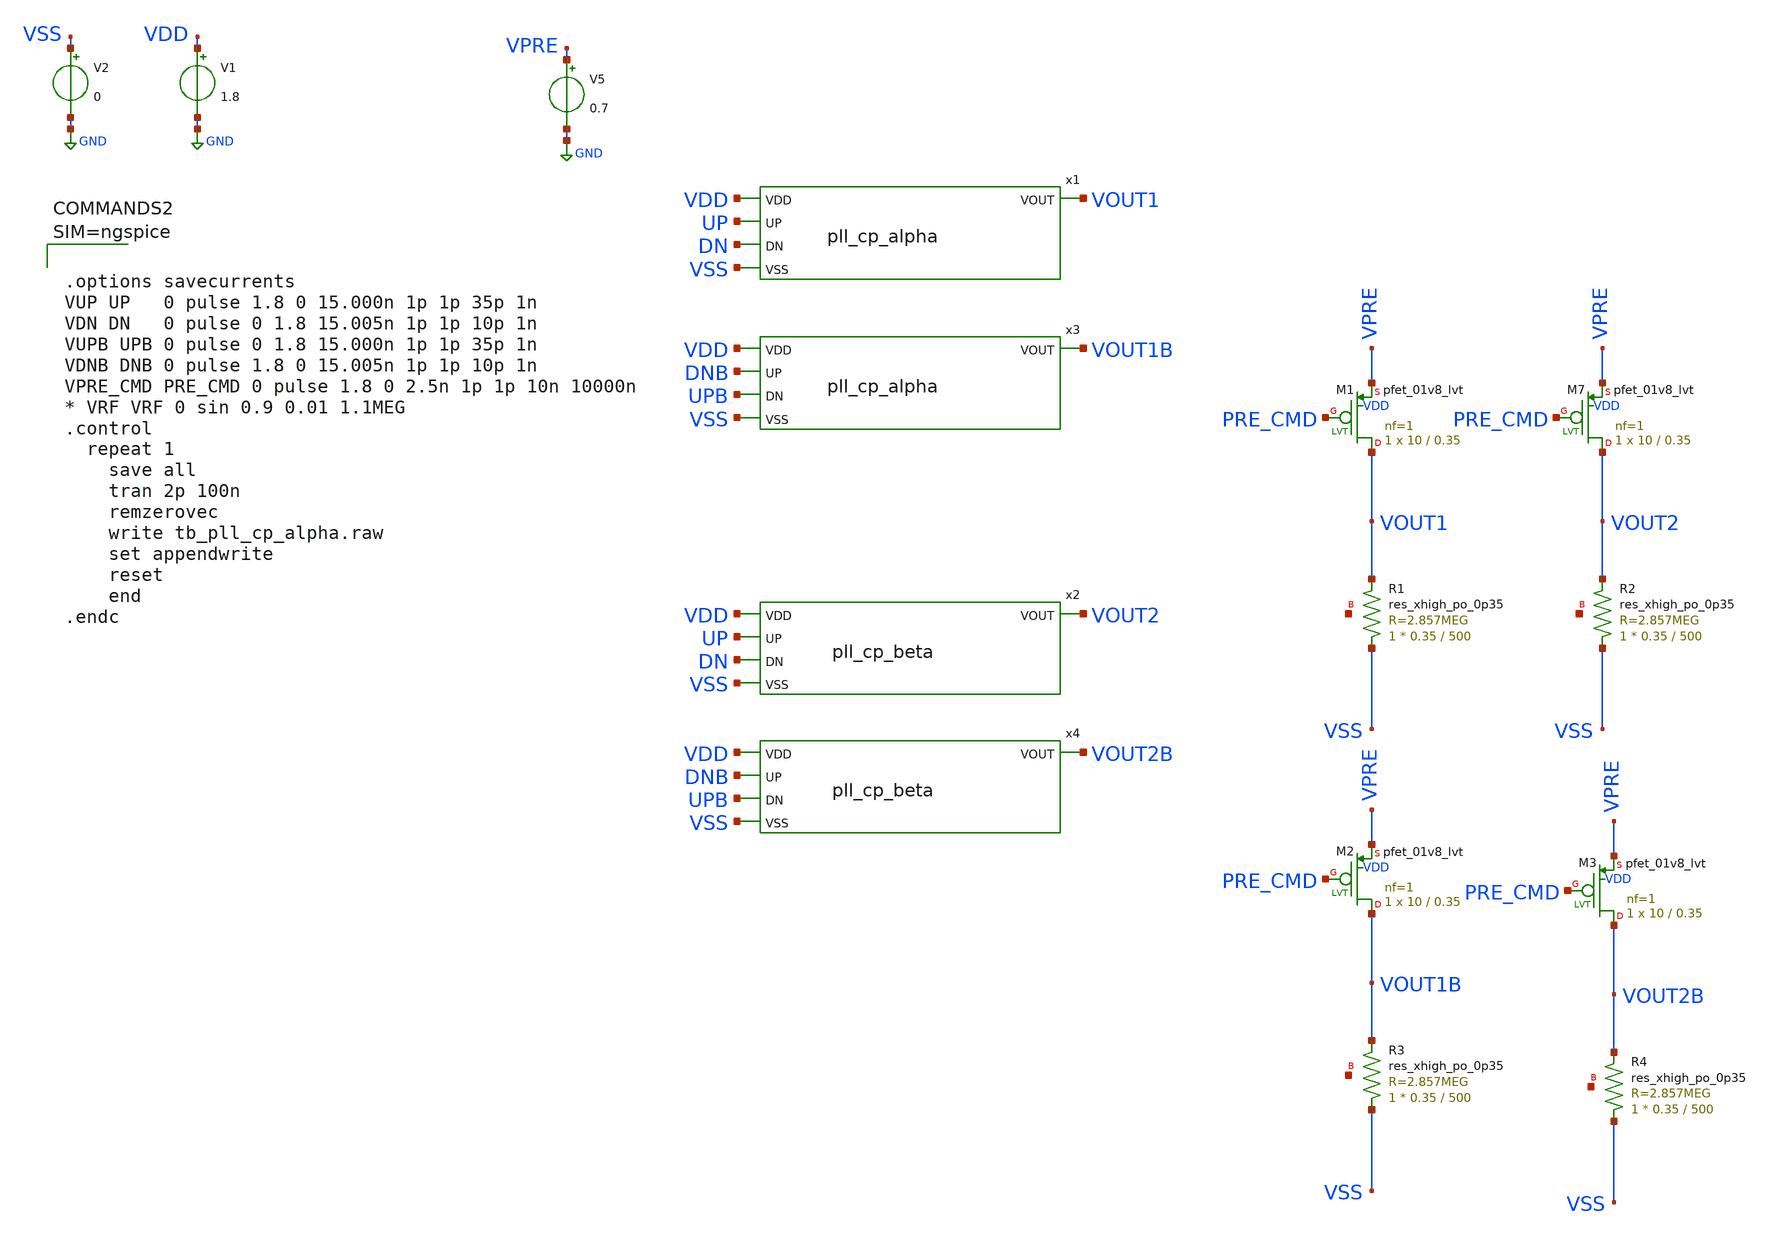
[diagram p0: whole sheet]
** sch_path: xschem/tb_pll_cp_alpha.sch
**.subckt tb_pll_cp_alpha
V1 VDD GND 1.8
V2 VSS GND 0
XR2 VSS VOUT2 net1 sky130_fd_pr__res_xhigh_po_0p35 L=500 mult=1 m=1
XM7 VOUT2 PRE_CMD VPRE VDD sky130_fd_pr__pfet_01v8_lvt L=0.35 W=10 nf=1 ad='int((nf+1)/2) * W/nf * 0.29'
+ as='int((nf+2)/2) * W/nf * 0.29' pd='2*int((nf+1)/2) * (W/nf + 0.29)' ps='2*int((nf+2)/2) * (W/nf + 0.29)'
+ nrd='0.29 / W' nrs='0.29 / W' sa=0 sb=0 sd=0 mult=1 m=1
V5 VPRE GND 0.7
x1 VDD UP DN VOUT1 VSS pll_cp_alpha
x2 VDD UP DN VOUT2 VSS pll_cp_beta
XR1 VSS VOUT1 net2 sky130_fd_pr__res_xhigh_po_0p35 L=500 mult=1 m=1
XM1 VOUT1 PRE_CMD VPRE VDD sky130_fd_pr__pfet_01v8_lvt L=0.35 W=10 nf=1 ad='int((nf+1)/2) * W/nf * 0.29'
+ as='int((nf+2)/2) * W/nf * 0.29' pd='2*int((nf+1)/2) * (W/nf + 0.29)' ps='2*int((nf+2)/2) * (W/nf + 0.29)'
+ nrd='0.29 / W' nrs='0.29 / W' sa=0 sb=0 sd=0 mult=1 m=1
x3 VDD DNB UPB VOUT1B VSS pll_cp_alpha
XR3 VSS VOUT1B net3 sky130_fd_pr__res_xhigh_po_0p35 L=500 mult=1 m=1
XM2 VOUT1B PRE_CMD VPRE VDD sky130_fd_pr__pfet_01v8_lvt L=0.35 W=10 nf=1 ad='int((nf+1)/2) * W/nf * 0.29'
+ as='int((nf+2)/2) * W/nf * 0.29' pd='2*int((nf+1)/2) * (W/nf + 0.29)' ps='2*int((nf+2)/2) * (W/nf + 0.29)'
+ nrd='0.29 / W' nrs='0.29 / W' sa=0 sb=0 sd=0 mult=1 m=1
x4 VDD DNB UPB VOUT2B VSS pll_cp_beta
XR4 VSS VOUT2B net4 sky130_fd_pr__res_xhigh_po_0p35 L=500 mult=1 m=1
XM3 VOUT2B PRE_CMD VPRE VDD sky130_fd_pr__pfet_01v8_lvt L=0.35 W=10 nf=1 ad='int((nf+1)/2) * W/nf * 0.29'
+ as='int((nf+2)/2) * W/nf * 0.29' pd='2*int((nf+1)/2) * (W/nf + 0.29)' ps='2*int((nf+2)/2) * (W/nf + 0.29)'
+ nrd='0.29 / W' nrs='0.29 / W' sa=0 sb=0 sd=0 mult=1 m=1
**** begin user architecture code

** opencircuitdesign pdks install
.lib $::SKYWATER_MODELS/sky130.lib.spice tt_mm





.options savecurrents
VUP UP   0 pulse 1.8 0 15.000n 1p 1p 35p 1n
VDN DN   0 pulse 0 1.8 15.005n 1p 1p 10p 1n
VUPB UPB 0 pulse 0 1.8 15.000n 1p 1p 35p 1n
VDNB DNB 0 pulse 1.8 0 15.005n 1p 1p 10p 1n
VPRE_CMD PRE_CMD 0 pulse 1.8 0 2.5n 1p 1p 10n 10000n
* VRF VRF 0 sin 0.9 0.01 1.1MEG
.control
  repeat 1
    save all
    tran 2p 100n
    remzerovec
    write tb_pll_cp_alpha.raw
    set appendwrite
    reset
    end
.endc



**** end user architecture code
**.ends

* expanding   symbol:  pll_cp_alpha.sym # of pins=5
** sym_path: xschem/pll_cp_alpha.sym
** sch_path: xschem/pll_cp_alpha.sch
.subckt pll_cp_alpha VDD UP DN VOUT VSS
*.ipin UP
*.opin VOUT
*.ipin DN
*.ipin VDD
*.ipin VSS
XM5 VDD DN VLOW VSS sky130_fd_pr__nfet_01v8_lvt L=0.35 W=5 nf=1 ad='int((nf+1)/2) * W/nf * 0.29' as='int((nf+2)/2) * W/nf * 0.29'
+ pd='2*int((nf+1)/2) * (W/nf + 0.29)' ps='2*int((nf+2)/2) * (W/nf + 0.29)' nrd='0.29 / W' nrs='0.29 / W'
+ sa=0 sb=0 sd=0 mult=1 m=1
XM6 net2 VBL net5 VSS sky130_fd_pr__nfet_01v8_lvt L=0.35 W=5 nf=1 ad='int((nf+1)/2) * W/nf * 0.29' as='int((nf+2)/2) * W/nf * 0.29'
+ pd='2*int((nf+1)/2) * (W/nf + 0.29)' ps='2*int((nf+2)/2) * (W/nf + 0.29)' nrd='0.29 / W' nrs='0.29 / W'
+ sa=0 sb=0 sd=0 mult=1 m=1
XM10 net1 net3 VSS VSS sky130_fd_pr__nfet_01v8_lvt L=1 W=2 nf=1 ad='int((nf+1)/2) * W/nf * 0.29' as='int((nf+2)/2) * W/nf * 0.29'
+ pd='2*int((nf+1)/2) * (W/nf + 0.29)' ps='2*int((nf+2)/2) * (W/nf + 0.29)' nrd='0.29 / W' nrs='0.29 / W'
+ sa=0 sb=0 sd=0 mult=1 m=1
vbias1 VLOW net1 0
.save i(vbias1)
XM1 net2 VBH net6 VDD sky130_fd_pr__pfet_01v8_lvt L=0.35 W=10 nf=1 ad='int((nf+1)/2) * W/nf * 0.29' as='int((nf+2)/2) * W/nf * 0.29'
+ pd='2*int((nf+1)/2) * (W/nf + 0.29)' ps='2*int((nf+2)/2) * (W/nf + 0.29)' nrd='0.29 / W' nrs='0.29 / W'
+ sa=0 sb=0 sd=0 mult=1 m=1
XM2 VSS UP VHIGH VDD sky130_fd_pr__pfet_01v8_lvt L=0.35 W=10 nf=1 ad='int((nf+1)/2) * W/nf * 0.29' as='int((nf+2)/2) * W/nf * 0.29'
+ pd='2*int((nf+1)/2) * (W/nf + 0.29)' ps='2*int((nf+2)/2) * (W/nf + 0.29)' nrd='0.29 / W' nrs='0.29 / W'
+ sa=0 sb=0 sd=0 mult=1 m=1
XC1 VOUT VSS sky130_fd_pr__cap_mim_m3_1 W=20 L=20 MF=1 m=1
XM11 net3 net3 VSS VSS sky130_fd_pr__nfet_01v8_lvt L=1 W=2 nf=1 ad='int((nf+1)/2) * W/nf * 0.29' as='int((nf+2)/2) * W/nf * 0.29'
+ pd='2*int((nf+1)/2) * (W/nf + 0.29)' ps='2*int((nf+2)/2) * (W/nf + 0.29)' nrd='0.29 / W' nrs='0.29 / W'
+ sa=0 sb=0 sd=0 mult=1 m=1
XR4 net3 net4 net7 sky130_fd_pr__res_xhigh_po_0p35 L=30 mult=1 m=1
XM3 VHIGH net4 VDD VDD sky130_fd_pr__pfet_01v8_lvt L=1 W=4 nf=1 ad='int((nf+1)/2) * W/nf * 0.29' as='int((nf+2)/2) * W/nf * 0.29'
+ pd='2*int((nf+1)/2) * (W/nf + 0.29)' ps='2*int((nf+2)/2) * (W/nf + 0.29)' nrd='0.29 / W' nrs='0.29 / W'
+ sa=0 sb=0 sd=0 mult=1 m=1
XM4 net4 net4 VDD VDD sky130_fd_pr__pfet_01v8_lvt L=1 W=4 nf=1 ad='int((nf+1)/2) * W/nf * 0.29' as='int((nf+2)/2) * W/nf * 0.29'
+ pd='2*int((nf+1)/2) * (W/nf + 0.29)' ps='2*int((nf+2)/2) * (W/nf + 0.29)' nrd='0.29 / W' nrs='0.29 / W'
+ sa=0 sb=0 sd=0 mult=1 m=1
V3 VBL VSS 0.8
vclow net5 VLOW 0
.save i(vclow)
vchigh VHIGH net6 0
.save i(vchigh)
V4 VBH VSS 1.0
XR1 VOUT net2 net8 sky130_fd_pr__res_xhigh_po_0p35 L=1 mult=1 m=1
XC2 net2 VSS sky130_fd_pr__cap_mim_m3_1 W=1 L=1 MF=1 m=1
.ends


* expanding   symbol:  pll_cp_beta.sym # of pins=5
** sym_path: xschem/pll_cp_beta.sym
** sch_path: xschem/pll_cp_beta.sch
.subckt pll_cp_beta VDD UP DN VOUT VSS
*.ipin UP
*.ipin DN
*.opin VOUT
*.ipin VDD
*.ipin VSS
XM6 net2 DN net5 VSS sky130_fd_pr__nfet_01v8_lvt L=0.35 W=1 nf=1 ad='int((nf+1)/2) * W/nf * 0.29' as='int((nf+2)/2) * W/nf * 0.29'
+ pd='2*int((nf+1)/2) * (W/nf + 0.29)' ps='2*int((nf+2)/2) * (W/nf + 0.29)' nrd='0.29 / W' nrs='0.29 / W'
+ sa=0 sb=0 sd=0 mult=1 m=1
XM10 net1 net3 VSS VSS sky130_fd_pr__nfet_01v8_lvt L=1 W=2 nf=1 ad='int((nf+1)/2) * W/nf * 0.29' as='int((nf+2)/2) * W/nf * 0.29'
+ pd='2*int((nf+1)/2) * (W/nf + 0.29)' ps='2*int((nf+2)/2) * (W/nf + 0.29)' nrd='0.29 / W' nrs='0.29 / W'
+ sa=0 sb=0 sd=0 mult=1 m=1
vbias1 VLOW net1 0
.save i(vbias1)
XM1 net2 UP net6 VDD sky130_fd_pr__pfet_01v8_lvt L=0.35 W=3 nf=1 ad='int((nf+1)/2) * W/nf * 0.29' as='int((nf+2)/2) * W/nf * 0.29'
+ pd='2*int((nf+1)/2) * (W/nf + 0.29)' ps='2*int((nf+2)/2) * (W/nf + 0.29)' nrd='0.29 / W' nrs='0.29 / W'
+ sa=0 sb=0 sd=0 mult=1 m=1
XC1 VOUT VSS sky130_fd_pr__cap_mim_m3_1 W=20 L=20 MF=1 m=1
XM11 net3 net3 VSS VSS sky130_fd_pr__nfet_01v8_lvt L=1 W=2 nf=1 ad='int((nf+1)/2) * W/nf * 0.29' as='int((nf+2)/2) * W/nf * 0.29'
+ pd='2*int((nf+1)/2) * (W/nf + 0.29)' ps='2*int((nf+2)/2) * (W/nf + 0.29)' nrd='0.29 / W' nrs='0.29 / W'
+ sa=0 sb=0 sd=0 mult=1 m=1
XR4 net3 net4 net7 sky130_fd_pr__res_xhigh_po_0p35 L=20 mult=1 m=1
XM3 VHIGH net4 VDD VDD sky130_fd_pr__pfet_01v8_lvt L=1 W=4 nf=1 ad='int((nf+1)/2) * W/nf * 0.29' as='int((nf+2)/2) * W/nf * 0.29'
+ pd='2*int((nf+1)/2) * (W/nf + 0.29)' ps='2*int((nf+2)/2) * (W/nf + 0.29)' nrd='0.29 / W' nrs='0.29 / W'
+ sa=0 sb=0 sd=0 mult=1 m=1
XM4 net4 net4 VDD VDD sky130_fd_pr__pfet_01v8_lvt L=1 W=4 nf=1 ad='int((nf+1)/2) * W/nf * 0.29' as='int((nf+2)/2) * W/nf * 0.29'
+ pd='2*int((nf+1)/2) * (W/nf + 0.29)' ps='2*int((nf+2)/2) * (W/nf + 0.29)' nrd='0.29 / W' nrs='0.29 / W'
+ sa=0 sb=0 sd=0 mult=1 m=1
vclow net5 VLOW 0
.save i(vclow)
vchigh VHIGH net6 0
.save i(vchigh)
XC2 net2 VSS sky130_fd_pr__cap_mim_m3_1 W=1 L=1 MF=1 m=1
XR1 VOUT net2 net8 sky130_fd_pr__res_xhigh_po_0p35 L=10 mult=1 m=1
.ends

.GLOBAL GND
.end
